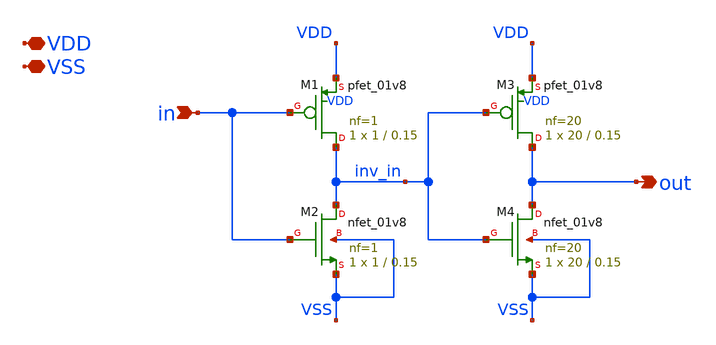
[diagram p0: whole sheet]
** sch_path: xschem/double_inverter.sch
**.subckt double_inverter VDD VSS in out
*.iopin VDD
*.iopin VSS
*.ipin in
*.opin out
XM1 inv_in in VDD VDD sky130_fd_pr__pfet_01v8 L=0.15 W=1 nf=1 ad='int((nf+1)/2) * W/nf * 0.29' as='int((nf+2)/2) * W/nf * 0.29'
+ pd='2*int((nf+1)/2) * (W/nf + 0.29)' ps='2*int((nf+2)/2) * (W/nf + 0.29)' nrd='0.29 / W' nrs='0.29 / W'
+ sa=0 sb=0 sd=0 mult=1 m=1
XM2 inv_in in VSS VSS sky130_fd_pr__nfet_01v8 L=0.15 W=1 nf=1 ad='int((nf+1)/2) * W/nf * 0.29' as='int((nf+2)/2) * W/nf * 0.29'
+ pd='2*int((nf+1)/2) * (W/nf + 0.29)' ps='2*int((nf+2)/2) * (W/nf + 0.29)' nrd='0.29 / W' nrs='0.29 / W'
+ sa=0 sb=0 sd=0 mult=1 m=1
XM3 out inv_in VDD VDD sky130_fd_pr__pfet_01v8 L=0.15 W=20 nf=20 ad='int((nf+1)/2) * W/nf * 0.29' as='int((nf+2)/2) * W/nf * 0.29'
+ pd='2*int((nf+1)/2) * (W/nf + 0.29)' ps='2*int((nf+2)/2) * (W/nf + 0.29)' nrd='0.29 / W' nrs='0.29 / W'
+ sa=0 sb=0 sd=0 mult=1 m=1
XM4 out inv_in VSS VSS sky130_fd_pr__nfet_01v8 L=0.15 W=20 nf=20 ad='int((nf+1)/2) * W/nf * 0.29' as='int((nf+2)/2) * W/nf * 0.29'
+ pd='2*int((nf+1)/2) * (W/nf + 0.29)' ps='2*int((nf+2)/2) * (W/nf + 0.29)' nrd='0.29 / W' nrs='0.29 / W'
+ sa=0 sb=0 sd=0 mult=1 m=1
**.ends
.end
